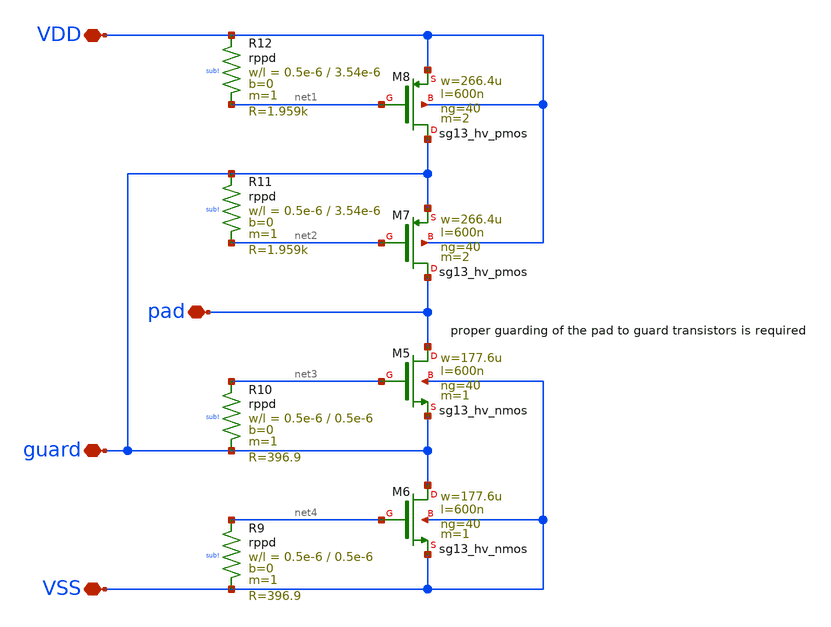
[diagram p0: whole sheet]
** sch_path: trident_test_structures/design_data/xschem/IOPadAnalogGuardLayer/clamps_guard_layer_x2_what.sch
**.subckt clamps_guard_layer_x2_what VSS VDD pad guard
*.iopin VSS
*.iopin VDD
*.iopin pad
*.iopin guard
XM5 pad net3 guard VSS sg13_hv_nmos w=177.6u l=600n ng=40 m=1 mm_ok=1
XM6 guard net4 VSS VSS sg13_hv_nmos w=177.6u l=600n ng=40 m=1 mm_ok=1
XM7 pad net2 guard VDD sg13_hv_pmos w=266.4u l=600n ng=40 m=2 mm_ok=1
XR9 net4 VSS sub! rppd w=0.5e-6 l=0.5e-6 m=1 b=0 mm_ok=1
XR10 net3 guard sub! rppd w=0.5e-6 l=0.5e-6 m=1 b=0 mm_ok=1
XR11 guard net2 sub! rppd w=0.5e-6 l=3.54e-6 m=1 b=0 mm_ok=1
XR12 VDD net1 sub! rppd w=0.5e-6 l=3.54e-6 m=1 b=0 mm_ok=1
XM8 guard net1 VDD VDD sg13_hv_pmos w=266.4u l=600n ng=40 m=2 mm_ok=1
**.ends
.end
